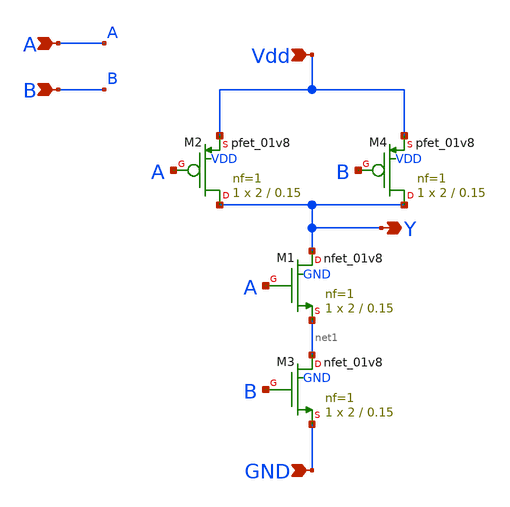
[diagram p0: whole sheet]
** sch_path: 2/src/nandlab.sch
**.subckt nandlab Y GND A Vdd B
*.opin Y
*.ipin GND
*.ipin A
*.ipin Vdd
*.ipin B
XM1 Y A net1 GND sky130_fd_pr__nfet_01v8 L=0.15 W=2 nf=1 ad='int((1 + 1)/2) * 2 / 1 * 0.29' as='int((1 + 2)/2) * 2 / 1 * 0.29'
+ pd='2*int((1 + 1)/2) * (2 / 1 + 0.29)' ps='2*int((1 + 2)/2) * (2 / 1 + 0.29)' nrd='0.29 / 2 ' nrs='0.29 / 2 '
+ sa=0 sb=0 sd=0 mult=1 m=1
XM2 Y A Vdd VDD sky130_fd_pr__pfet_01v8 L=0.15 W=2 nf=1 ad='int((1 + 1)/2) * 2 / 1 * 0.29' as='int((1 + 2)/2) * 2 / 1 * 0.29'
+ pd='2*int((1 + 1)/2) * (2 / 1 + 0.29)' ps='2*int((1 + 2)/2) * (2 / 1 + 0.29)' nrd='0.29 / 2 ' nrs='0.29 / 2 '
+ sa=0 sb=0 sd=0 mult=1 m=1
XM3 net1 B GND GND sky130_fd_pr__nfet_01v8 L=0.15 W=2 nf=1 ad='int((1 + 1)/2) * 2 / 1 * 0.29' as='int((1 + 2)/2) * 2 / 1 * 0.29'
+ pd='2*int((1 + 1)/2) * (2 / 1 + 0.29)' ps='2*int((1 + 2)/2) * (2 / 1 + 0.29)' nrd='0.29 / 2 ' nrs='0.29 / 2 '
+ sa=0 sb=0 sd=0 mult=1 m=1
XM4 Y B Vdd VDD sky130_fd_pr__pfet_01v8 L=0.15 W=2 nf=1 ad='int((1 + 1)/2) * 2 / 1 * 0.29' as='int((1 + 2)/2) * 2 / 1 * 0.29'
+ pd='2*int((1 + 1)/2) * (2 / 1 + 0.29)' ps='2*int((1 + 2)/2) * (2 / 1 + 0.29)' nrd='0.29 / 2 ' nrs='0.29 / 2 '
+ sa=0 sb=0 sd=0 mult=1 m=1
**.ends
.end
